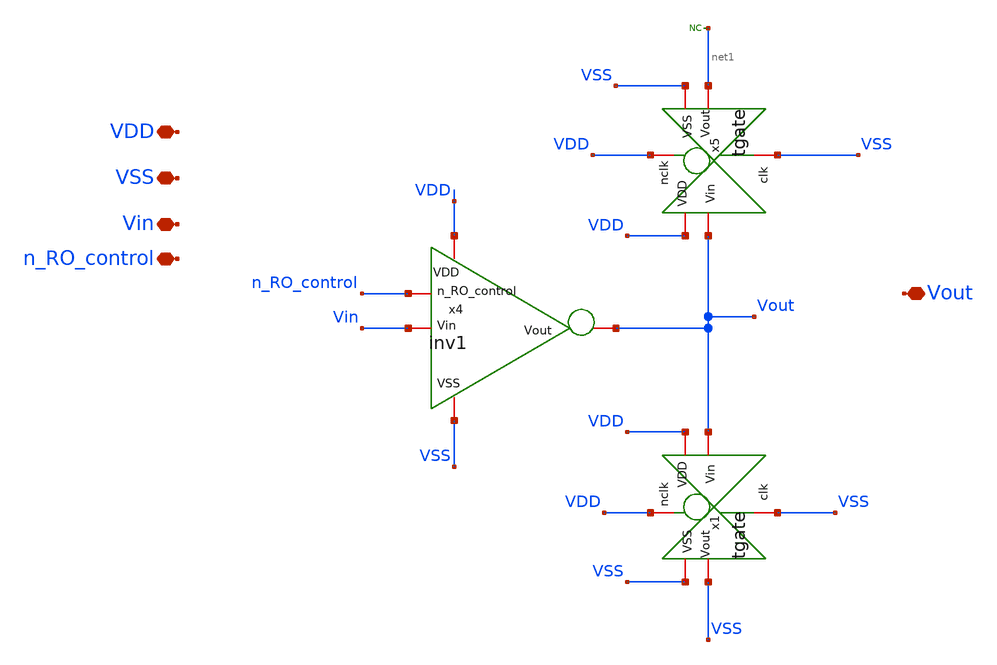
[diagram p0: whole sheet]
** sch_path: unic_cass_wrapper_user_project/ROs_reliability/rovcel4.sch
**.subckt rovcel4 VDD VSS Vin n_RO_control Vout
*.iopin VDD
*.iopin VSS
*.iopin Vin
*.iopin n_RO_control
*.iopin Vout
* noconn #net1
x4 n_RO_control VDD VSS Vin Vout inv1
x1 VDD VDD Vout VSS VSS VSS tgate
x5 VDD VDD Vout net1 VSS VSS tgate
**.ends

* expanding   symbol:  inv1.sym # of pins=5
** sym_path: inv1.sym
** sch_path: inv1.sch
.subckt inv1 n_RO_control VDD VSS Vin Vout
*.iopin VDD
*.iopin VSS
*.iopin Vin
*.iopin Vout
*.iopin n_RO_control
XM1 net1 n_RO_control VDD VDD sg13_lv_pmos w=3.4u l=0.45u ng=1 m=12 mm_ok=1
XM5 Vout Vin net1 VDD sg13_lv_pmos w=3.4u l=0.45u ng=1 m=4 mm_ok=1
XM2 VSS Vin Vout VSS sg13_lv_nmos w=1.3u l=0.45u ng=1 m=4 mm_ok=1
.ends


* expanding   symbol:  tgate.sym # of pins=6
** sym_path: tgate.sym
** sch_path: tgate.sch
.subckt tgate nclk VDD Vin Vout VSS clk
*.iopin nclk
*.iopin clk
*.iopin VDD
*.iopin VSS
*.iopin Vout
*.iopin Vin
XM3 Vout nclk Vin VDD sg13_lv_pmos w=3.4u l=0.45u ng=1 m=1 mm_ok=1
XM1 Vout clk Vin VSS sg13_lv_nmos w=1.3u l=0.45u ng=1 m=1 mm_ok=1
.ends

.end
